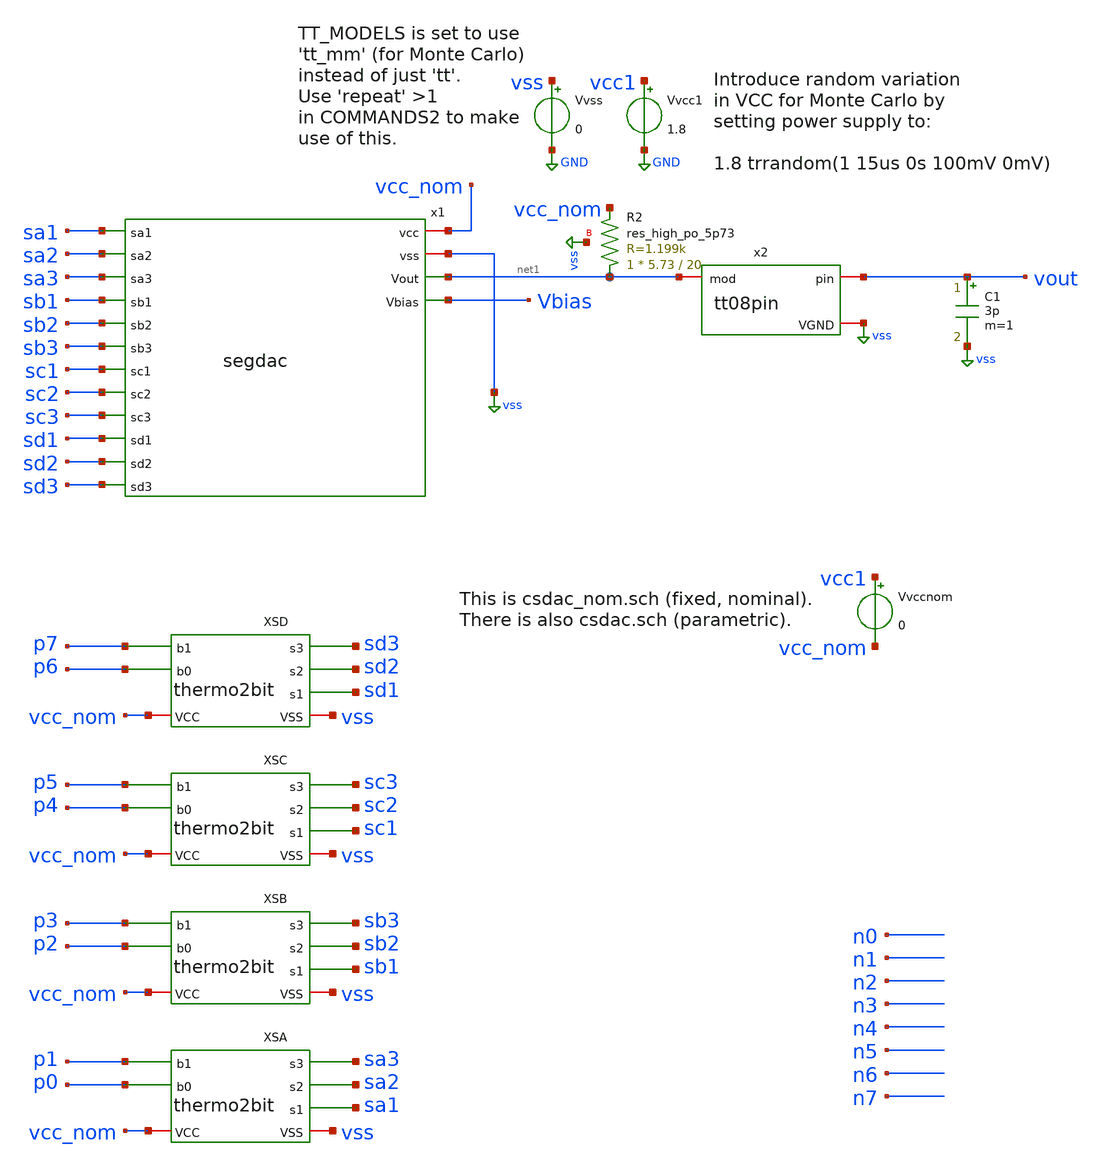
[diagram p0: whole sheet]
** sch_path: xschem/tb_segdac.sch
**.subckt tb_segdac
Vvcc1 vcc1 GND 1.8
Vvss vss GND 0
Vvccnom vcc1 vcc_nom 0
x1 sa1 vcc_nom sa2 vss sa3 net1 sb1 sb2 Vbias sb3 sc1 sc2 sc3 sd1 sd2 sd3 segdac
XSA vcc_nom vss sa3 p1 sa2 sa1 p0 thermo2bit
XSB vcc_nom vss sb3 p3 sb2 sb1 p2 thermo2bit
XSC vcc_nom vss sc3 p5 sc2 sc1 p4 thermo2bit
XSD vcc_nom vss sd3 p7 sd2 sd1 p6 thermo2bit
XR2 net1 vcc_nom vss sky130_fd_pr__res_high_po_5p73 L=20 mult=1 m=1
x2 vout net1 vss tt08pin
C1 vout vss 3p m=1
**** begin user architecture code




.param singlebits=0
.IF (singlebits == 1)
* Mode to just test each binary-weighted level:
Vxp0 p0 GND pulse 0v 1.8v 1u 1n 1n 1u 10u
Vxp1 p1 GND pulse 0v 1.8v 2u 1n 1n 1u 10u
Vxp2 p2 GND pulse 0v 1.8v 3u 1n 1n 1u 10u
Vxp3 p3 GND pulse 0v 1.8v 4u 1n 1n 1u 10u
Vxp4 p4 GND pulse 0v 1.8v 5u 1n 1n 1u 10u
Vxp5 p5 GND pulse 0v 1.8v 6u 1n 1n 1u 10u
Vxp6 p6 GND pulse 0v 1.8v 7u 1n 1n 1u 10u
Vxp7 p7 GND pulse 0v 1.8v 8u 1n 1n 1u 10u
Vxn0 n0 GND pulse 1.8v 0v 1u 1n 1n 1u 10u
Vxn1 n1 GND pulse 1.8v 0v 2u 1n 1n 1u 10u
Vxn2 n2 GND pulse 1.8v 0v 3u 1n 1n 1u 10u
Vxn3 n3 GND pulse 1.8v 0v 4u 1n 1n 1u 10u
Vxn4 n4 GND pulse 1.8v 0v 5u 1n 1n 1u 10u
Vxn5 n5 GND pulse 1.8v 0v 6u 1n 1n 1u 10u
Vxn6 n6 GND pulse 1.8v 0v 7u 1n 1n 1u 10u
Vxn7 n7 GND pulse 1.8v 0v 8u 1n 1n 1u 10u
.ELSEIF (singlebits == 0)
* Mode to test full 0..255 trange:
Vxp0 p0 GND pulse 1.8v 0v 0n 1n 1n 39n 80n
Vxp1 p1 GND pulse 1.8v 0v 0n 1n 1n 79n 160n
Vxp2 p2 GND pulse 1.8v 0v 0n 1n 1n 159n 320n
Vxp3 p3 GND pulse 1.8v 0v 0n 1n 1n 319n 640n
Vxp4 p4 GND pulse 1.8v 0v 0n 1n 1n 639n 1280n
Vxp5 p5 GND pulse 1.8v 0v 0n 1n 1n 1279n 2560n
Vxp6 p6 GND pulse 1.8v 0v 0n 1n 1n 2559n 5120n
Vxp7 p7 GND pulse 1.8v 0v 0n 1n 1n 5119n 10240n
Vxn0 n0 GND pulse 0v 1.8v 0n 1n 1n 39n 80n
Vxn1 n1 GND pulse 0v 1.8v 0n 1n 1n 79n 160n
Vxn2 n2 GND pulse 0v 1.8v 0n 1n 1n 159n 320n
Vxn3 n3 GND pulse 0v 1.8v 0n 1n 1n 319n 640n
Vxn4 n4 GND pulse 0v 1.8v 0n 1n 1n 639n 1280n
Vxn5 n5 GND pulse 0v 1.8v 0n 1n 1n 1279n 2560n
Vxn6 n6 GND pulse 0v 1.8v 0n 1n 1n 2559n 5120n
Vxn7 n7 GND pulse 0v 1.8v 0n 1n 1n 5119n 10240n
.ENDIF

.options savecurrents
.control

  * If using Monte Carlo, change to repeat to (say) 5:
  repeat 1
    save all
    tran 1n 12.8u
    write tb_segdac.raw i(vvss) vcc1 vbias vout i(vvccnom)
    + p0 p1 p2 p3 p4 p5 p6 p7
    + sa1 sa2 sa3 sb1 sb2 sb3 sc1 sc2 sc3 sd1 sd2 sd3
    * + i(voutload)
    set appendwrite
    reset
  end

*  save all
*  *reset
*  *alterparam MPW=4
*  *alterparam MMW=4
*  tran 1n 12.8u
*  write 11.raw i(vvcc) i(vvss) vpos vneg vbias

*  set appendwrite
*  alterparam MPW=4
*  alterparam MMW=4
*  reset
*  tran 1n 12.8u
*  write 11.raw i(vvcc) i(vvss) vpos vneg vbias

.endc




.lib $::SKYWATER_MODELS/sky130.lib.spice tt
.include $::SKYWATER_STDCELLS/sky130_fd_sc_hd.spice

**** end user architecture code
**.ends

* expanding   symbol:  segdac.sym # of pins=16
** sym_path: xschem/segdac.sym
** sch_path: xschem/segdac.sch
.subckt segdac sa1 vcc sa2 vss sa3 Vout sb1 sb2 Vbias sb3 sc1 sc2 sc3 sd1 sd2 sd3
*.iopin vcc
*.iopin vss
*.opin Vout
*.opin Vbias
*.ipin sa1
*.ipin sa2
*.ipin sa3
*.ipin sb1
*.ipin sb2
*.ipin sb3
*.ipin sc1
*.ipin sc2
*.ipin sc3
*.ipin sd1
*.ipin sd2
*.ipin sd3
XMprog Vbias vss vcc vcc sky130_fd_pr__pfet_01v8 L=0.7 W=0.5 nf=1 ad='int((nf+1)/2) * W/nf * 0.29' as='int((nf+2)/2) * W/nf * 0.29'
+ pd='2*int((nf+1)/2) * (W/nf + 0.29)' ps='2*int((nf+2)/2) * (W/nf + 0.29)' nrd='0.29 / W' nrs='0.29 / W'
+ sa=0 sb=0 sd=0 mult=1 m=1
XMmirror Vbias Vbias vss vss sky130_fd_pr__nfet_01v8 L=0.5 W=1 nf=1 ad='int((nf+1)/2) * W/nf * 0.29'
+ as='int((nf+2)/2) * W/nf * 0.29' pd='2*int((nf+1)/2) * (W/nf + 0.29)' ps='2*int((nf+2)/2) * (W/nf + 0.29)'
+ nrd='0.29 / W' nrs='0.29 / W' sa=0 sb=0 sd=0 mult=1 m=1
XMia1 net1 Vbias vss vss sky130_fd_pr__nfet_01v8 L=2.4 W=0.5 nf=1 ad='int((nf+1)/2) * W/nf * 0.29' as='int((nf+2)/2) * W/nf * 0.29'
+ pd='2*int((nf+1)/2) * (W/nf + 0.29)' ps='2*int((nf+2)/2) * (W/nf + 0.29)' nrd='0.29 / W' nrs='0.29 / W'
+ sa=0 sb=0 sd=0 mult=1 m=1
XMia2 net2 Vbias vss vss sky130_fd_pr__nfet_01v8 L=2.4 W=0.5 nf=1 ad='int((nf+1)/2) * W/nf * 0.29' as='int((nf+2)/2) * W/nf * 0.29'
+ pd='2*int((nf+1)/2) * (W/nf + 0.29)' ps='2*int((nf+2)/2) * (W/nf + 0.29)' nrd='0.29 / W' nrs='0.29 / W'
+ sa=0 sb=0 sd=0 mult=1 m=1
XMia3 net3 Vbias vss vss sky130_fd_pr__nfet_01v8 L=2.4 W=0.5 nf=1 ad='int((nf+1)/2) * W/nf * 0.29' as='int((nf+2)/2) * W/nf * 0.29'
+ pd='2*int((nf+1)/2) * (W/nf + 0.29)' ps='2*int((nf+2)/2) * (W/nf + 0.29)' nrd='0.29 / W' nrs='0.29 / W'
+ sa=0 sb=0 sd=0 mult=1 m=1
XMsa1 Vout sa1 net1 vss sky130_fd_pr__nfet_01v8 L=0.15 W=0.5 nf=1 ad='int((nf+1)/2) * W/nf * 0.29' as='int((nf+2)/2) * W/nf * 0.29'
+ pd='2*int((nf+1)/2) * (W/nf + 0.29)' ps='2*int((nf+2)/2) * (W/nf + 0.29)' nrd='0.29 / W' nrs='0.29 / W'
+ sa=0 sb=0 sd=0 mult=1 m=1
XMsa2 Vout sa2 net2 vss sky130_fd_pr__nfet_01v8 L=0.15 W=0.5 nf=1 ad='int((nf+1)/2) * W/nf * 0.29' as='int((nf+2)/2) * W/nf * 0.29'
+ pd='2*int((nf+1)/2) * (W/nf + 0.29)' ps='2*int((nf+2)/2) * (W/nf + 0.29)' nrd='0.29 / W' nrs='0.29 / W'
+ sa=0 sb=0 sd=0 mult=1 m=1
XMsa3 Vout sa3 net3 vss sky130_fd_pr__nfet_01v8 L=0.15 W=0.5 nf=1 ad='int((nf+1)/2) * W/nf * 0.29' as='int((nf+2)/2) * W/nf * 0.29'
+ pd='2*int((nf+1)/2) * (W/nf + 0.29)' ps='2*int((nf+2)/2) * (W/nf + 0.29)' nrd='0.29 / W' nrs='0.29 / W'
+ sa=0 sb=0 sd=0 mult=1 m=1
XMib1 net4 Vbias vss vss sky130_fd_pr__nfet_01v8 L=1.2 W=1.1 nf=1 ad='int((nf+1)/2) * W/nf * 0.29' as='int((nf+2)/2) * W/nf * 0.29'
+ pd='2*int((nf+1)/2) * (W/nf + 0.29)' ps='2*int((nf+2)/2) * (W/nf + 0.29)' nrd='0.29 / W' nrs='0.29 / W'
+ sa=0 sb=0 sd=0 mult=1 m=1
XMib2 net5 Vbias vss vss sky130_fd_pr__nfet_01v8 L=1.2 W=1.1 nf=1 ad='int((nf+1)/2) * W/nf * 0.29' as='int((nf+2)/2) * W/nf * 0.29'
+ pd='2*int((nf+1)/2) * (W/nf + 0.29)' ps='2*int((nf+2)/2) * (W/nf + 0.29)' nrd='0.29 / W' nrs='0.29 / W'
+ sa=0 sb=0 sd=0 mult=1 m=1
XMib3 net6 Vbias vss vss sky130_fd_pr__nfet_01v8 L=1.2 W=1.1 nf=1 ad='int((nf+1)/2) * W/nf * 0.29' as='int((nf+2)/2) * W/nf * 0.29'
+ pd='2*int((nf+1)/2) * (W/nf + 0.29)' ps='2*int((nf+2)/2) * (W/nf + 0.29)' nrd='0.29 / W' nrs='0.29 / W'
+ sa=0 sb=0 sd=0 mult=1 m=1
XMsb1 Vout sb1 net4 vss sky130_fd_pr__nfet_01v8 L=0.15 W=0.5 nf=1 ad='int((nf+1)/2) * W/nf * 0.29' as='int((nf+2)/2) * W/nf * 0.29'
+ pd='2*int((nf+1)/2) * (W/nf + 0.29)' ps='2*int((nf+2)/2) * (W/nf + 0.29)' nrd='0.29 / W' nrs='0.29 / W'
+ sa=0 sb=0 sd=0 mult=1 m=1
XMsb2 Vout sb2 net5 vss sky130_fd_pr__nfet_01v8 L=0.15 W=0.5 nf=1 ad='int((nf+1)/2) * W/nf * 0.29' as='int((nf+2)/2) * W/nf * 0.29'
+ pd='2*int((nf+1)/2) * (W/nf + 0.29)' ps='2*int((nf+2)/2) * (W/nf + 0.29)' nrd='0.29 / W' nrs='0.29 / W'
+ sa=0 sb=0 sd=0 mult=1 m=1
XMsb3 Vout sb3 net6 vss sky130_fd_pr__nfet_01v8 L=0.15 W=0.5 nf=1 ad='int((nf+1)/2) * W/nf * 0.29' as='int((nf+2)/2) * W/nf * 0.29'
+ pd='2*int((nf+1)/2) * (W/nf + 0.29)' ps='2*int((nf+2)/2) * (W/nf + 0.29)' nrd='0.29 / W' nrs='0.29 / W'
+ sa=0 sb=0 sd=0 mult=1 m=1
XMic1 net7 Vbias vss vss sky130_fd_pr__nfet_01v8 L=0.25 W=1.8 nf=1 ad='int((nf+1)/2) * W/nf * 0.29' as='int((nf+2)/2) * W/nf * 0.29'
+ pd='2*int((nf+1)/2) * (W/nf + 0.29)' ps='2*int((nf+2)/2) * (W/nf + 0.29)' nrd='0.29 / W' nrs='0.29 / W'
+ sa=0 sb=0 sd=0 mult=1 m=1
XMic2 net8 Vbias vss vss sky130_fd_pr__nfet_01v8 L=0.25 W=1.8 nf=1 ad='int((nf+1)/2) * W/nf * 0.29' as='int((nf+2)/2) * W/nf * 0.29'
+ pd='2*int((nf+1)/2) * (W/nf + 0.29)' ps='2*int((nf+2)/2) * (W/nf + 0.29)' nrd='0.29 / W' nrs='0.29 / W'
+ sa=0 sb=0 sd=0 mult=1 m=1
XMic3 net9 Vbias vss vss sky130_fd_pr__nfet_01v8 L=0.25 W=1.8 nf=1 ad='int((nf+1)/2) * W/nf * 0.29' as='int((nf+2)/2) * W/nf * 0.29'
+ pd='2*int((nf+1)/2) * (W/nf + 0.29)' ps='2*int((nf+2)/2) * (W/nf + 0.29)' nrd='0.29 / W' nrs='0.29 / W'
+ sa=0 sb=0 sd=0 mult=1 m=1
XMsc1 Vout sc1 net7 vss sky130_fd_pr__nfet_01v8 L=0.15 W=1.9 nf=1 ad='int((nf+1)/2) * W/nf * 0.29' as='int((nf+2)/2) * W/nf * 0.29'
+ pd='2*int((nf+1)/2) * (W/nf + 0.29)' ps='2*int((nf+2)/2) * (W/nf + 0.29)' nrd='0.29 / W' nrs='0.29 / W'
+ sa=0 sb=0 sd=0 mult=1 m=1
XMsc2 Vout sc2 net8 vss sky130_fd_pr__nfet_01v8 L=0.15 W=1.9 nf=1 ad='int((nf+1)/2) * W/nf * 0.29' as='int((nf+2)/2) * W/nf * 0.29'
+ pd='2*int((nf+1)/2) * (W/nf + 0.29)' ps='2*int((nf+2)/2) * (W/nf + 0.29)' nrd='0.29 / W' nrs='0.29 / W'
+ sa=0 sb=0 sd=0 mult=1 m=1
XMsc3 Vout sc3 net9 vss sky130_fd_pr__nfet_01v8 L=0.15 W=1.9 nf=1 ad='int((nf+1)/2) * W/nf * 0.29' as='int((nf+2)/2) * W/nf * 0.29'
+ pd='2*int((nf+1)/2) * (W/nf + 0.29)' ps='2*int((nf+2)/2) * (W/nf + 0.29)' nrd='0.29 / W' nrs='0.29 / W'
+ sa=0 sb=0 sd=0 mult=1 m=1
XMid1 net10 Vbias vss vss sky130_fd_pr__nfet_01v8 L=0.15 W=4 nf=1 ad='int((nf+1)/2) * W/nf * 0.29' as='int((nf+2)/2) * W/nf * 0.29'
+ pd='2*int((nf+1)/2) * (W/nf + 0.29)' ps='2*int((nf+2)/2) * (W/nf + 0.29)' nrd='0.29 / W' nrs='0.29 / W'
+ sa=0 sb=0 sd=0 mult=1 m=1
XMid2 net11 Vbias vss vss sky130_fd_pr__nfet_01v8 L=0.15 W=4 nf=1 ad='int((nf+1)/2) * W/nf * 0.29' as='int((nf+2)/2) * W/nf * 0.29'
+ pd='2*int((nf+1)/2) * (W/nf + 0.29)' ps='2*int((nf+2)/2) * (W/nf + 0.29)' nrd='0.29 / W' nrs='0.29 / W'
+ sa=0 sb=0 sd=0 mult=1 m=1
XMid3 net12 Vbias vss vss sky130_fd_pr__nfet_01v8 L=0.15 W=4 nf=1 ad='int((nf+1)/2) * W/nf * 0.29' as='int((nf+2)/2) * W/nf * 0.29'
+ pd='2*int((nf+1)/2) * (W/nf + 0.29)' ps='2*int((nf+2)/2) * (W/nf + 0.29)' nrd='0.29 / W' nrs='0.29 / W'
+ sa=0 sb=0 sd=0 mult=1 m=1
XMsd1 Vout sd1 net10 vss sky130_fd_pr__nfet_01v8 L=0.15 W=5.7 nf=1 ad='int((nf+1)/2) * W/nf * 0.29' as='int((nf+2)/2) * W/nf * 0.29'
+ pd='2*int((nf+1)/2) * (W/nf + 0.29)' ps='2*int((nf+2)/2) * (W/nf + 0.29)' nrd='0.29 / W' nrs='0.29 / W'
+ sa=0 sb=0 sd=0 mult=1 m=1
XMsd2 Vout sd2 net11 vss sky130_fd_pr__nfet_01v8 L=0.15 W=5.7 nf=1 ad='int((nf+1)/2) * W/nf * 0.29' as='int((nf+2)/2) * W/nf * 0.29'
+ pd='2*int((nf+1)/2) * (W/nf + 0.29)' ps='2*int((nf+2)/2) * (W/nf + 0.29)' nrd='0.29 / W' nrs='0.29 / W'
+ sa=0 sb=0 sd=0 mult=1 m=1
XMsd3 Vout sd3 net12 vss sky130_fd_pr__nfet_01v8 L=0.15 W=5.7 nf=1 ad='int((nf+1)/2) * W/nf * 0.29' as='int((nf+2)/2) * W/nf * 0.29'
+ pd='2*int((nf+1)/2) * (W/nf + 0.29)' ps='2*int((nf+2)/2) * (W/nf + 0.29)' nrd='0.29 / W' nrs='0.29 / W'
+ sa=0 sb=0 sd=0 mult=1 m=1
.ends


* expanding   symbol:  thermo2bit.sym # of pins=7
** sym_path: xschem/thermo2bit.sym
** sch_path: xschem/thermo2bit.sch
.subckt thermo2bit VCC VSS s3 b1 s2 s1 b0
*.ipin b1
*.opin s2
*.ipin b0
*.opin s3
*.iopin VCC
*.iopin VSS
*.opin s1
R1 s2 b1 0 m=1
XM1 net1 b0 VCC VCC sky130_fd_pr__pfet_01v8 L=0.15 W=1 nf=1 ad='int((nf+1)/2) * W/nf * 0.29' as='int((nf+2)/2) * W/nf * 0.29'
+ pd='2*int((nf+1)/2) * (W/nf + 0.29)' ps='2*int((nf+2)/2) * (W/nf + 0.29)' nrd='0.29 / W' nrs='0.29 / W'
+ sa=0 sb=0 sd=0 mult=1 m=1
XM2 net1 b0 net2 VSS sky130_fd_pr__nfet_01v8 L=0.15 W=0.5 nf=1 ad='int((nf+1)/2) * W/nf * 0.29' as='int((nf+2)/2) * W/nf * 0.29'
+ pd='2*int((nf+1)/2) * (W/nf + 0.29)' ps='2*int((nf+2)/2) * (W/nf + 0.29)' nrd='0.29 / W' nrs='0.29 / W'
+ sa=0 sb=0 sd=0 mult=1 m=1
XM3 net1 b1 VCC VCC sky130_fd_pr__pfet_01v8 L=0.15 W=1 nf=1 ad='int((nf+1)/2) * W/nf * 0.29' as='int((nf+2)/2) * W/nf * 0.29'
+ pd='2*int((nf+1)/2) * (W/nf + 0.29)' ps='2*int((nf+2)/2) * (W/nf + 0.29)' nrd='0.29 / W' nrs='0.29 / W'
+ sa=0 sb=0 sd=0 mult=1 m=1
XM4 net2 b1 VSS VSS sky130_fd_pr__nfet_01v8 L=0.15 W=0.5 nf=1 ad='int((nf+1)/2) * W/nf * 0.29' as='int((nf+2)/2) * W/nf * 0.29'
+ pd='2*int((nf+1)/2) * (W/nf + 0.29)' ps='2*int((nf+2)/2) * (W/nf + 0.29)' nrd='0.29 / W' nrs='0.29 / W'
+ sa=0 sb=0 sd=0 mult=1 m=1
XM5 s3 net1 VCC VCC sky130_fd_pr__pfet_01v8 L=0.15 W=1 nf=1 ad='int((nf+1)/2) * W/nf * 0.29' as='int((nf+2)/2) * W/nf * 0.29'
+ pd='2*int((nf+1)/2) * (W/nf + 0.29)' ps='2*int((nf+2)/2) * (W/nf + 0.29)' nrd='0.29 / W' nrs='0.29 / W'
+ sa=0 sb=0 sd=0 mult=1 m=1
XM6 s3 net1 VSS VSS sky130_fd_pr__nfet_01v8 L=0.15 W=0.5 nf=1 ad='int((nf+1)/2) * W/nf * 0.29' as='int((nf+2)/2) * W/nf * 0.29'
+ pd='2*int((nf+1)/2) * (W/nf + 0.29)' ps='2*int((nf+2)/2) * (W/nf + 0.29)' nrd='0.29 / W' nrs='0.29 / W'
+ sa=0 sb=0 sd=0 mult=1 m=1
XM11 s1 net3 VCC VCC sky130_fd_pr__pfet_01v8 L=0.15 W=1 nf=1 ad='int((nf+1)/2) * W/nf * 0.29' as='int((nf+2)/2) * W/nf * 0.29'
+ pd='2*int((nf+1)/2) * (W/nf + 0.29)' ps='2*int((nf+2)/2) * (W/nf + 0.29)' nrd='0.29 / W' nrs='0.29 / W'
+ sa=0 sb=0 sd=0 mult=1 m=1
XM12 s1 net3 VSS VSS sky130_fd_pr__nfet_01v8 L=0.15 W=0.5 nf=1 ad='int((nf+1)/2) * W/nf * 0.29' as='int((nf+2)/2) * W/nf * 0.29'
+ pd='2*int((nf+1)/2) * (W/nf + 0.29)' ps='2*int((nf+2)/2) * (W/nf + 0.29)' nrd='0.29 / W' nrs='0.29 / W'
+ sa=0 sb=0 sd=0 mult=1 m=1
XM7 net4 b0 VCC VCC sky130_fd_pr__pfet_01v8 L=0.15 W=1 nf=1 ad='int((nf+1)/2) * W/nf * 0.29' as='int((nf+2)/2) * W/nf * 0.29'
+ pd='2*int((nf+1)/2) * (W/nf + 0.29)' ps='2*int((nf+2)/2) * (W/nf + 0.29)' nrd='0.29 / W' nrs='0.29 / W'
+ sa=0 sb=0 sd=0 mult=1 m=1
XM8 net3 b1 net4 VCC sky130_fd_pr__pfet_01v8 L=0.15 W=1 nf=1 ad='int((nf+1)/2) * W/nf * 0.29' as='int((nf+2)/2) * W/nf * 0.29'
+ pd='2*int((nf+1)/2) * (W/nf + 0.29)' ps='2*int((nf+2)/2) * (W/nf + 0.29)' nrd='0.29 / W' nrs='0.29 / W'
+ sa=0 sb=0 sd=0 mult=1 m=1
XM9 net3 b0 VSS VSS sky130_fd_pr__nfet_01v8 L=0.15 W=0.5 nf=1 ad='int((nf+1)/2) * W/nf * 0.29' as='int((nf+2)/2) * W/nf * 0.29'
+ pd='2*int((nf+1)/2) * (W/nf + 0.29)' ps='2*int((nf+2)/2) * (W/nf + 0.29)' nrd='0.29 / W' nrs='0.29 / W'
+ sa=0 sb=0 sd=0 mult=1 m=1
XM10 net3 b1 VSS VSS sky130_fd_pr__nfet_01v8 L=0.15 W=0.5 nf=1 ad='int((nf+1)/2) * W/nf * 0.29' as='int((nf+2)/2) * W/nf * 0.29'
+ pd='2*int((nf+1)/2) * (W/nf + 0.29)' ps='2*int((nf+2)/2) * (W/nf + 0.29)' nrd='0.29 / W' nrs='0.29 / W'
+ sa=0 sb=0 sd=0 mult=1 m=1
.ends


* expanding   symbol:  tt08pin.sym # of pins=3
** sym_path: xschem/tt08pin.sym
** sch_path: xschem/tt08pin.sch
.subckt tt08pin pin mod VGND
*.iopin pin
*.iopin VGND
*.iopin mod
R1 net1 pin 1 m=1
C1 pin VGND 1p m=1
L1 net2 net1 1n m=1
V1 VAPWR VGND 3.3
C2 net2 VGND 2p m=1
R2 net3 net2 50 m=1
XM2 net3 VGND mod VAPWR sky130_fd_pr__pfet_g5v0d10v5 L=0.5 W=100 nf=20 ad='int((nf+1)/2) * W/nf * 0.29'
+ as='int((nf+2)/2) * W/nf * 0.29' pd='2*int((nf+1)/2) * (W/nf + 0.29)' ps='2*int((nf+2)/2) * (W/nf + 0.29)'
+ nrd='0.29 / W' nrs='0.29 / W' sa=0 sb=0 sd=0 mult=1 m=1
XM1 net3 VAPWR mod VGND sky130_fd_pr__nfet_g5v0d10v5 L=0.5 W=60 nf=12 ad='int((nf+1)/2) * W/nf * 0.29'
+ as='int((nf+2)/2) * W/nf * 0.29' pd='2*int((nf+1)/2) * (W/nf + 0.29)' ps='2*int((nf+2)/2) * (W/nf + 0.29)'
+ nrd='0.29 / W' nrs='0.29 / W' sa=0 sb=0 sd=0 mult=1 m=1
XM4 net3 VAPWR VGND VAPWR sky130_fd_pr__pfet_g5v0d10v5 L=0.5 W=100 nf=20 ad='int((nf+1)/2) * W/nf * 0.29'
+ as='int((nf+2)/2) * W/nf * 0.29' pd='2*int((nf+1)/2) * (W/nf + 0.29)' ps='2*int((nf+2)/2) * (W/nf + 0.29)'
+ nrd='0.29 / W' nrs='0.29 / W' sa=0 sb=0 sd=0 mult=15 m=15
XM3 net3 VGND VGND VGND sky130_fd_pr__nfet_g5v0d10v5 L=0.5 W=60 nf=12 ad='int((nf+1)/2) * W/nf * 0.29'
+ as='int((nf+2)/2) * W/nf * 0.29' pd='2*int((nf+1)/2) * (W/nf + 0.29)' ps='2*int((nf+2)/2) * (W/nf + 0.29)'
+ nrd='0.29 / W' nrs='0.29 / W' sa=0 sb=0 sd=0 mult=15 m=15
C3 mod VGND 250f m=1
.ends

.GLOBAL GND
.GLOBAL vss
.GLOBAL VGND
.GLOBAL VAPWR
.end
